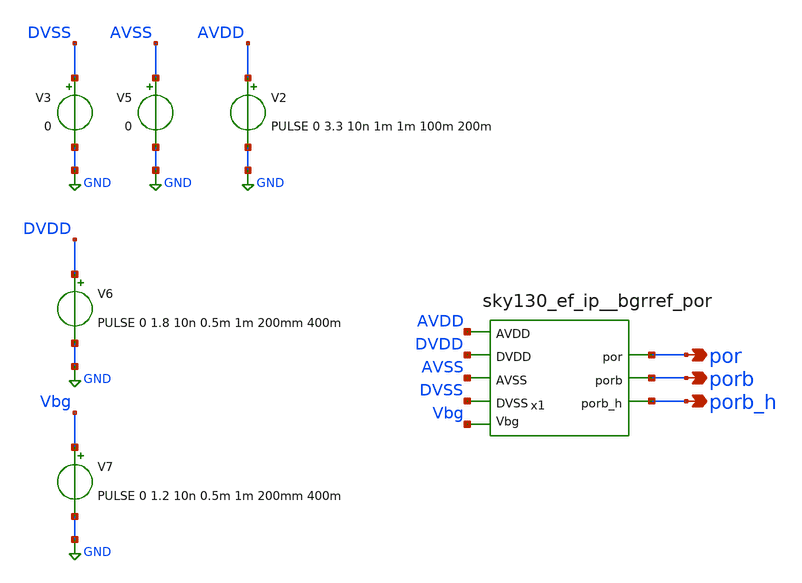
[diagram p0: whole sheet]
** sch_path: xschem/sky130_ef_ip__bgrref_por_tb.sch
**.subckt sky130_ef_ip__bgrref_por_tb por porb porb_h
*.opin por
*.opin porb
*.opin porb_h
x1 Vbg por AVSS AVDD DVDD porb DVSS porb_h VCC VSS sky130_ef_ip__bgrref_por W_N=1 L_N=0.2 W_P=1
+ L_P=0.2 m=1
V3 DVSS GND 0
V2 AVDD GND PULSE 0 3.3 10n 1m 1m 100m 200m
V5 AVSS GND 0
V6 DVDD GND PULSE 0 1.8 10n 0.5m 1m 200mm 400m
V7 Vbg GND PULSE 0 1.2 10n 0.5m 1m 200mm 400m
**** begin user architecture code
 .lib $::SKYWATER_MODELS/sky130.lib.spice tt

.include $::SKYWATER_STDCELLS/sky130_fd_sc_hd.spice



.options savecurrents
.control
save all
tran 1u 55m
plot AVDD por porb+6.8 porb_h+3.4
* write sky130_ef_ip__bgrref_por_tb.raw
*quit 0
.endc


**** end user architecture code
**.ends
.GLOBAL GND
.end
